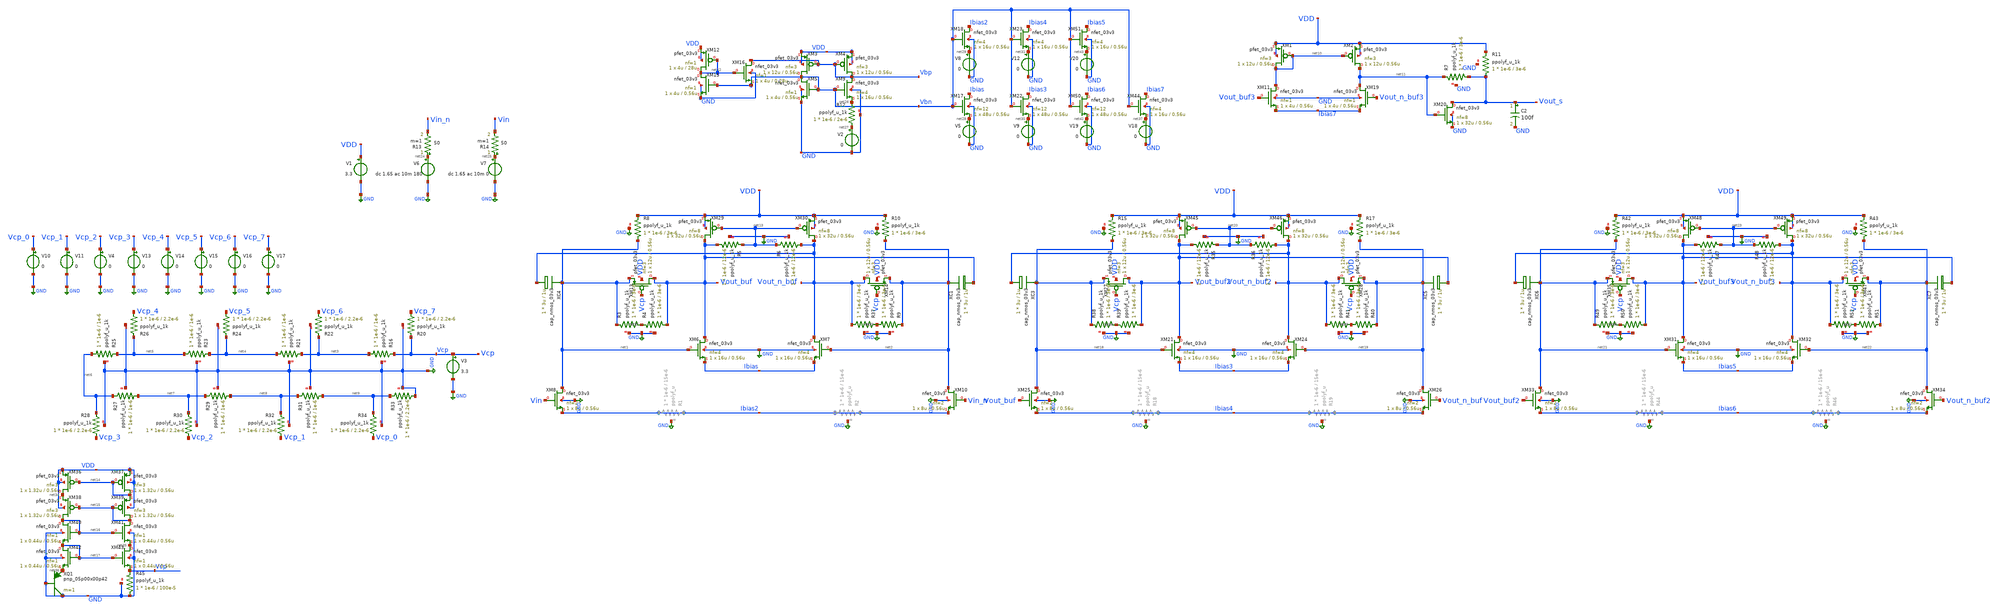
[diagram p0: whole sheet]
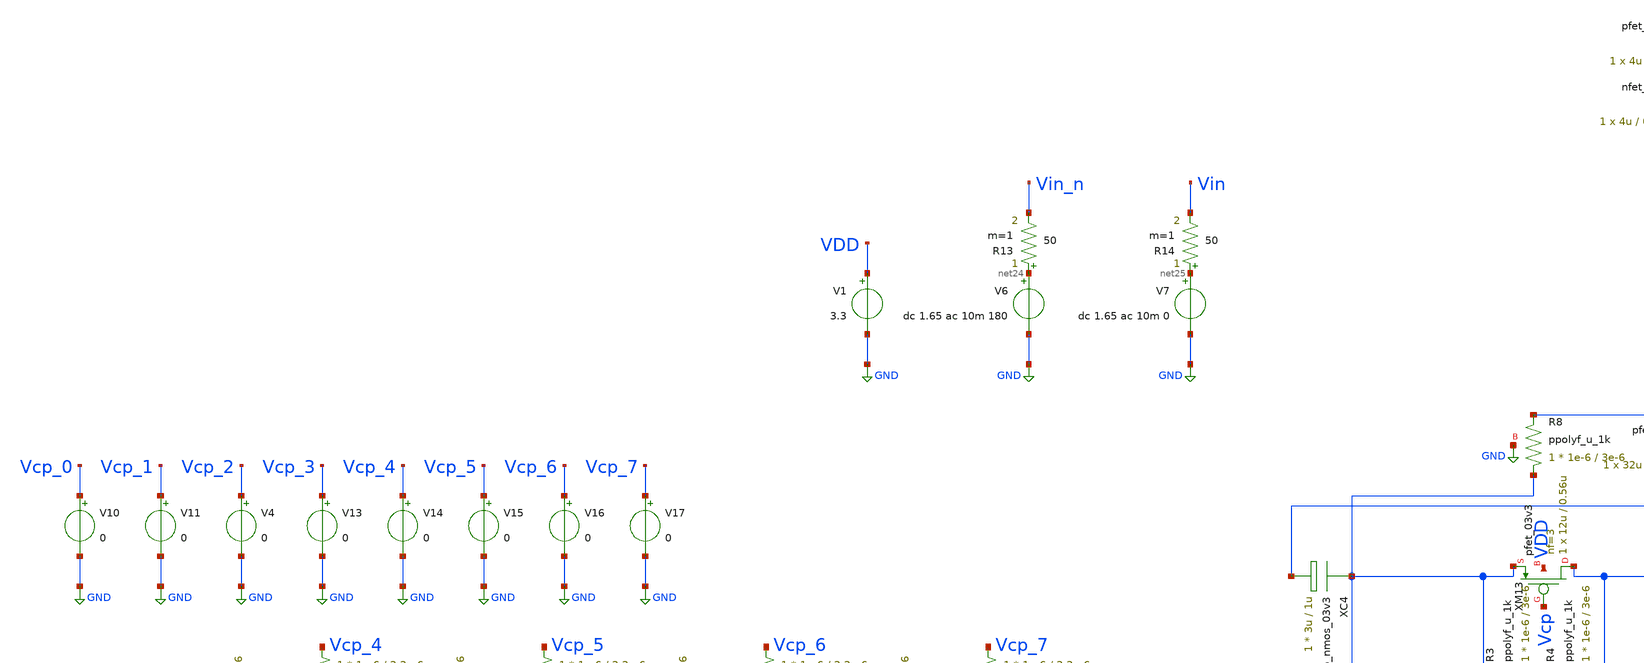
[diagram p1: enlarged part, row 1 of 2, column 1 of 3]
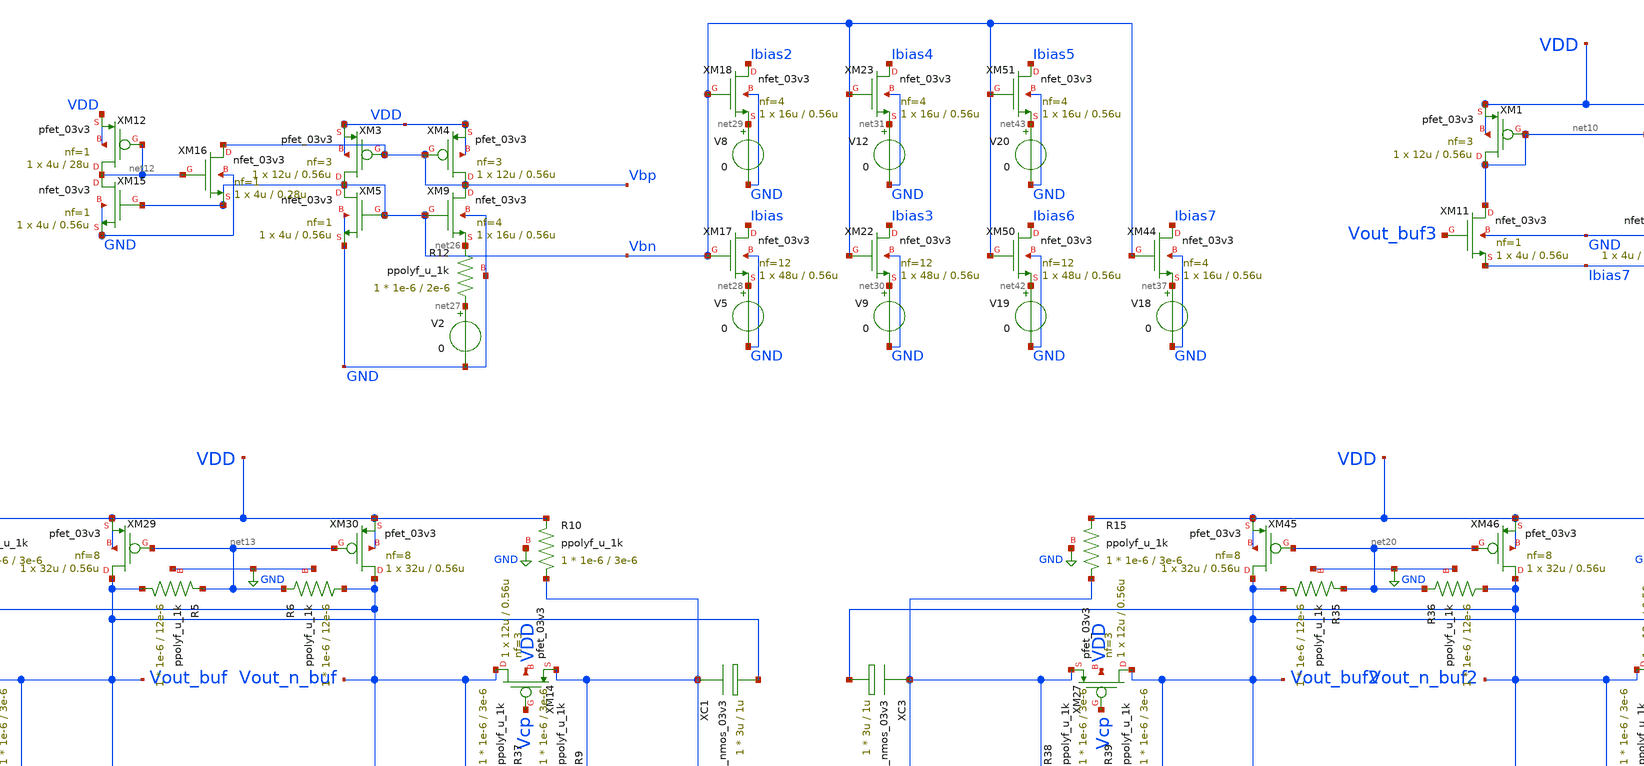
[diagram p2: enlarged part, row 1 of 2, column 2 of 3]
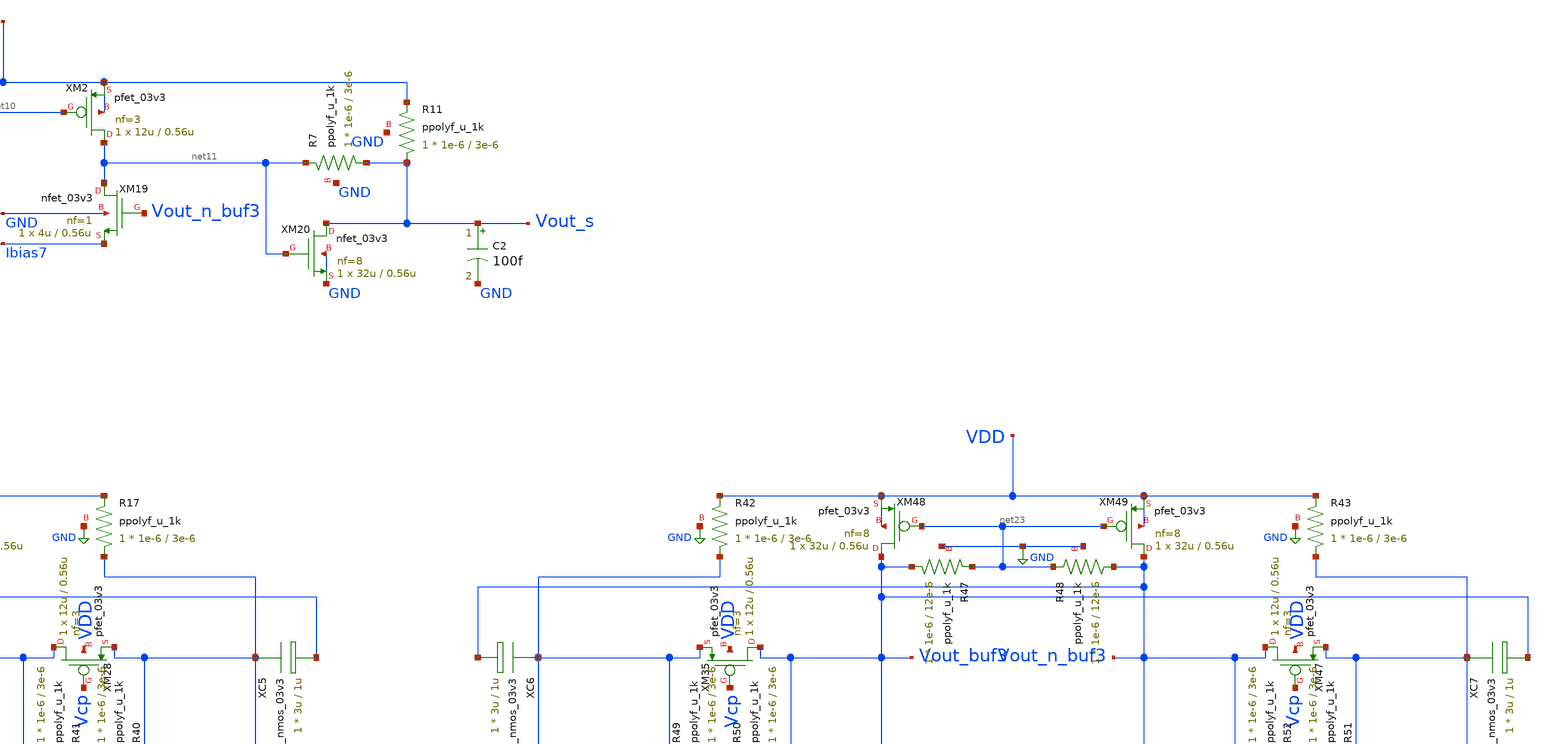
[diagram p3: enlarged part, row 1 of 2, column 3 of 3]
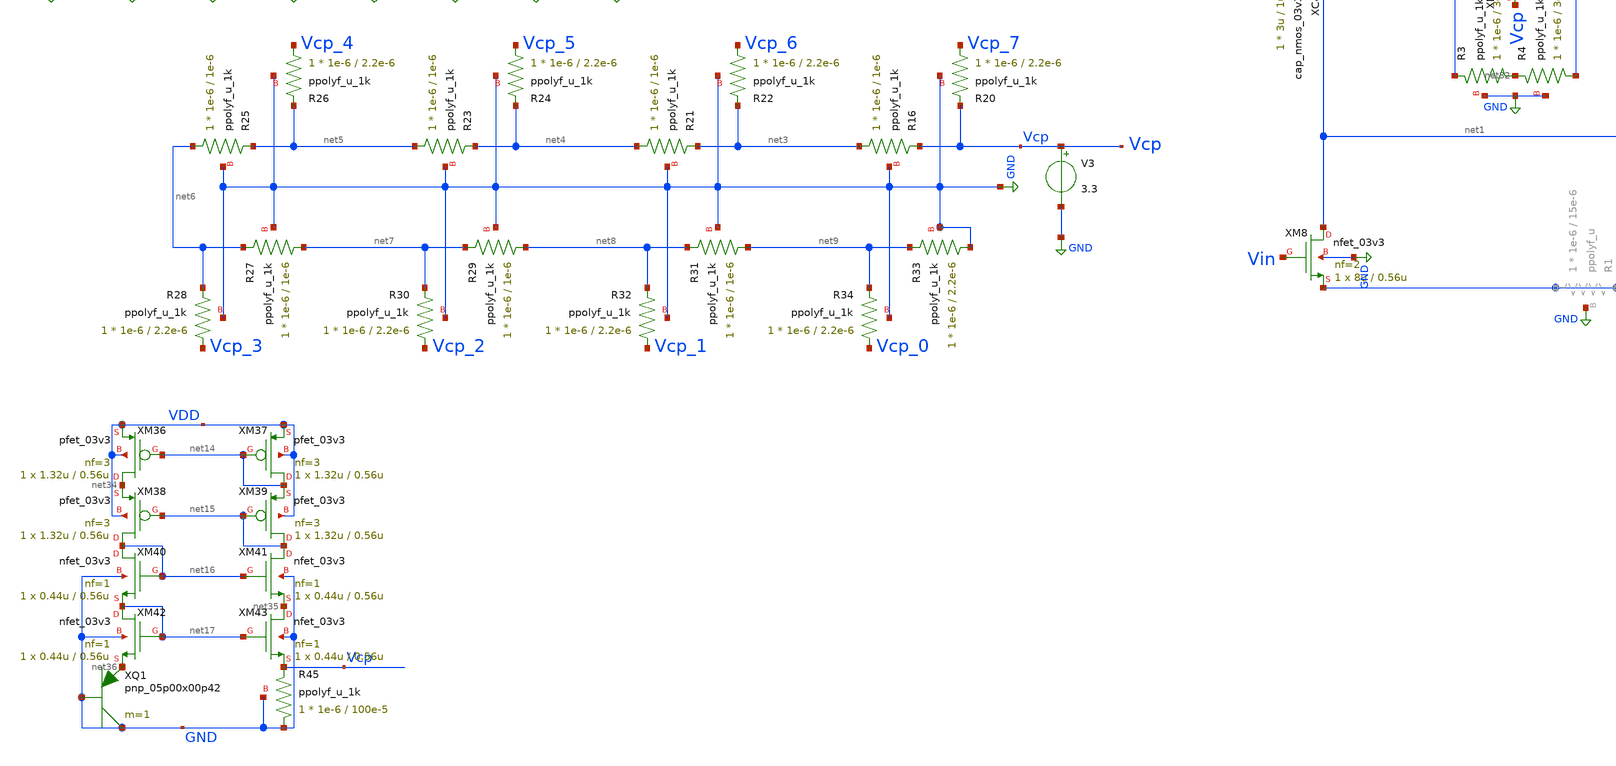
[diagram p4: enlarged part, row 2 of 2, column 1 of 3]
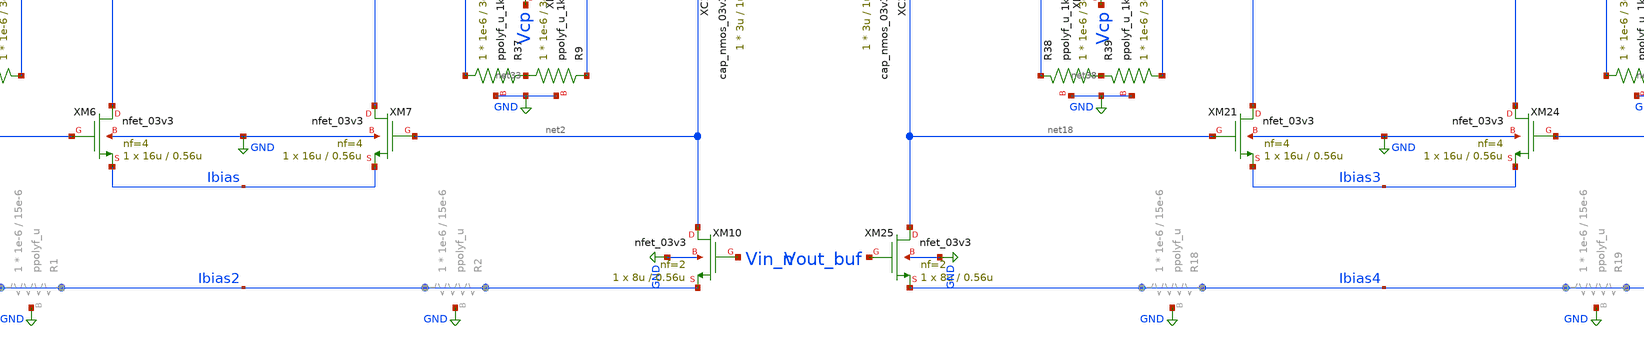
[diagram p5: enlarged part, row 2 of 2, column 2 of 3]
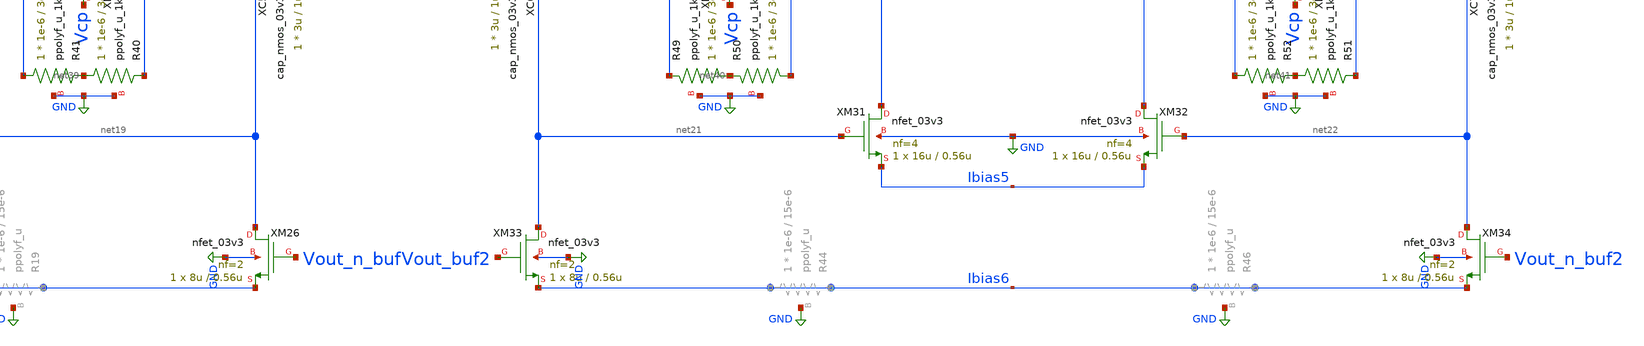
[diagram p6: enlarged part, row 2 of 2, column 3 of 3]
** sch_path: blocks/vga/vga.sch
**.subckt vga
V1 VDD GND 3.3
V6 net24 GND dc 1.65 ac 10m 180
XM6 Vout_buf net1 Ibias GND nfet_03v3 L=0.56u W=16u nf=4 ad='int((nf+1)/2) * W/nf * 0.18u' as='int((nf+2)/2) * W/nf * 0.18u'
+ pd='2*int((nf+1)/2) * (W/nf + 0.18u)' ps='2*int((nf+2)/2) * (W/nf + 0.18u)' nrd='0.18u / W' nrs='0.18u / W'
+ sa=0 sb=0 sd=0 m=1
XM7 Vout_n_buf net2 Ibias GND nfet_03v3 L=0.56u W=16u nf=4 ad='int((nf+1)/2) * W/nf * 0.18u' as='int((nf+2)/2) * W/nf * 0.18u'
+ pd='2*int((nf+1)/2) * (W/nf + 0.18u)' ps='2*int((nf+2)/2) * (W/nf + 0.18u)' nrd='0.18u / W' nrs='0.18u / W'
+ sa=0 sb=0 sd=0 m=1
XM8 net1 Vin Ibias2 GND nfet_03v3 L=0.56u W=8u nf=2 ad='int((nf+1)/2) * W/nf * 0.18u' as='int((nf+2)/2) * W/nf * 0.18u'
+ pd='2*int((nf+1)/2) * (W/nf + 0.18u)' ps='2*int((nf+2)/2) * (W/nf + 0.18u)' nrd='0.18u / W' nrs='0.18u / W'
+ sa=0 sb=0 sd=0 m=1
XM10 net2 Vin_n Ibias2 GND nfet_03v3 L=0.56u W=8u nf=2 ad='int((nf+1)/2) * W/nf * 0.18u' as='int((nf+2)/2) * W/nf * 0.18u'
+ pd='2*int((nf+1)/2) * (W/nf + 0.18u)' ps='2*int((nf+2)/2) * (W/nf + 0.18u)' nrd='0.18u / W' nrs='0.18u / W'
+ sa=0 sb=0 sd=0 m=1
V7 net25 GND dc 1.65 ac 10m 0
R14 net25 Vin 50 m=1
R13 net24 Vin_n 50 m=1
XR16 net3 Vcp GND ppolyf_u_1k r_width=1e-6 r_length=1e-6 m=1
XR20 Vcp_7 Vcp GND ppolyf_u_1k r_width=1e-6 r_length=2.2e-6 m=1
XR21 net4 net3 GND ppolyf_u_1k r_width=1e-6 r_length=1e-6 m=1
XR22 Vcp_6 net3 GND ppolyf_u_1k r_width=1e-6 r_length=2.2e-6 m=1
XR23 net5 net4 GND ppolyf_u_1k r_width=1e-6 r_length=1e-6 m=1
XR24 Vcp_5 net4 GND ppolyf_u_1k r_width=1e-6 r_length=2.2e-6 m=1
XR25 net6 net5 GND ppolyf_u_1k r_width=1e-6 r_length=1e-6 m=1
XR26 Vcp_4 net5 GND ppolyf_u_1k r_width=1e-6 r_length=2.2e-6 m=1
XR27 net7 net6 GND ppolyf_u_1k r_width=1e-6 r_length=1e-6 m=1
XR28 Vcp_3 net6 GND ppolyf_u_1k r_width=1e-6 r_length=2.2e-6 m=1
XR29 net8 net7 GND ppolyf_u_1k r_width=1e-6 r_length=1e-6 m=1
XR30 Vcp_2 net7 GND ppolyf_u_1k r_width=1e-6 r_length=2.2e-6 m=1
XR31 net9 net8 GND ppolyf_u_1k r_width=1e-6 r_length=1e-6 m=1
XR32 Vcp_1 net8 GND ppolyf_u_1k r_width=1e-6 r_length=2.2e-6 m=1
XR33 GND net9 GND ppolyf_u_1k r_width=1e-6 r_length=2.2e-6 m=1
XR34 Vcp_0 net9 GND ppolyf_u_1k r_width=1e-6 r_length=2.2e-6 m=1
V10 Vcp_0 GND 0
V11 Vcp_1 GND 0
V4 Vcp_2 GND 0
V13 Vcp_3 GND 0
V14 Vcp_4 GND 0
V15 Vcp_5 GND 0
V16 Vcp_6 GND 0
V17 Vcp_7 GND 0
V3 Vcp GND 3.3
XM13 Vout_buf Vcp net1 VDD pfet_03v3 L=0.56u W=12u nf=3 ad='int((nf+1)/2) * W/nf * 0.18u' as='int((nf+2)/2) * W/nf * 0.18u'
+ pd='2*int((nf+1)/2) * (W/nf + 0.18u)' ps='2*int((nf+2)/2) * (W/nf + 0.18u)' nrd='0.18u / W' nrs='0.18u / W'
+ sa=0 sb=0 sd=0 m=1
XM14 Vout_n_buf Vcp net2 VDD pfet_03v3 L=0.56u W=12u nf=3 ad='int((nf+1)/2) * W/nf * 0.18u' as='int((nf+2)/2) * W/nf * 0.18u'
+ pd='2*int((nf+1)/2) * (W/nf + 0.18u)' ps='2*int((nf+2)/2) * (W/nf + 0.18u)' nrd='0.18u / W' nrs='0.18u / W'
+ sa=0 sb=0 sd=0 m=1
XR8 net1 VDD GND ppolyf_u_1k r_width=1e-6 r_length=3e-6 m=1
XR10 net2 VDD GND ppolyf_u_1k r_width=1e-6 r_length=3e-6 m=1
XC4 net1 Vout_n_buf cap_nmos_03v3 c_width=3u c_length=1u m=1
XC1 net2 Vout_buf cap_nmos_03v3 c_width=3u c_length=1u m=1
XM11 net10 Vout_buf3 Ibias7 GND nfet_03v3 L=0.56u W=4u nf=1 ad='int((nf+1)/2) * W/nf * 0.18u' as='int((nf+2)/2) * W/nf * 0.18u'
+ pd='2*int((nf+1)/2) * (W/nf + 0.18u)' ps='2*int((nf+2)/2) * (W/nf + 0.18u)' nrd='0.18u / W' nrs='0.18u / W'
+ sa=0 sb=0 sd=0 m=1
XM19 net11 Vout_n_buf3 Ibias7 GND nfet_03v3 L=0.56u W=4u nf=1 ad='int((nf+1)/2) * W/nf * 0.18u' as='int((nf+2)/2) * W/nf * 0.18u'
+ pd='2*int((nf+1)/2) * (W/nf + 0.18u)' ps='2*int((nf+2)/2) * (W/nf + 0.18u)' nrd='0.18u / W' nrs='0.18u / W'
+ sa=0 sb=0 sd=0 m=1
XR7 Vout_s net11 GND ppolyf_u_1k r_width=1e-6 r_length=3e-6 m=1
XM20 Vout_s net11 GND GND nfet_03v3 L=0.56u W=32u nf=8 ad='int((nf+1)/2) * W/nf * 0.18u' as='int((nf+2)/2) * W/nf * 0.18u'
+ pd='2*int((nf+1)/2) * (W/nf + 0.18u)' ps='2*int((nf+2)/2) * (W/nf + 0.18u)' nrd='0.18u / W' nrs='0.18u / W'
+ sa=0 sb=0 sd=0 m=1
C2 Vout_s GND 100f m=1
XR11 Vout_s VDD GND ppolyf_u_1k r_width=1e-6 r_length=3e-6 m=1
XM1 net10 net10 VDD VDD pfet_03v3 L=0.56u W=12u nf=3 ad='int((nf+1)/2) * W/nf * 0.18u' as='int((nf+2)/2) * W/nf * 0.18u'
+ pd='2*int((nf+1)/2) * (W/nf + 0.18u)' ps='2*int((nf+2)/2) * (W/nf + 0.18u)' nrd='0.18u / W' nrs='0.18u / W'
+ sa=0 sb=0 sd=0 m=1
XM2 net11 net10 VDD VDD pfet_03v3 L=0.56u W=12u nf=3 ad='int((nf+1)/2) * W/nf * 0.18u' as='int((nf+2)/2) * W/nf * 0.18u'
+ pd='2*int((nf+1)/2) * (W/nf + 0.18u)' ps='2*int((nf+2)/2) * (W/nf + 0.18u)' nrd='0.18u / W' nrs='0.18u / W'
+ sa=0 sb=0 sd=0 m=1
XM3 Vbn Vbp VDD VDD pfet_03v3 L=0.56u W=12u nf=3 ad='int((nf+1)/2) * W/nf * 0.18u' as='int((nf+2)/2) * W/nf * 0.18u'
+ pd='2*int((nf+1)/2) * (W/nf + 0.18u)' ps='2*int((nf+2)/2) * (W/nf + 0.18u)' nrd='0.18u / W' nrs='0.18u / W'
+ sa=0 sb=0 sd=0 m=1
XM4 Vbp Vbp VDD VDD pfet_03v3 L=0.56u W=12u nf=3 ad='int((nf+1)/2) * W/nf * 0.18u' as='int((nf+2)/2) * W/nf * 0.18u'
+ pd='2*int((nf+1)/2) * (W/nf + 0.18u)' ps='2*int((nf+2)/2) * (W/nf + 0.18u)' nrd='0.18u / W' nrs='0.18u / W'
+ sa=0 sb=0 sd=0 m=1
XM5 Vbn Vbn GND GND nfet_03v3 L=0.56u W=4u nf=1 ad='int((nf+1)/2) * W/nf * 0.18u' as='int((nf+2)/2) * W/nf * 0.18u'
+ pd='2*int((nf+1)/2) * (W/nf + 0.18u)' ps='2*int((nf+2)/2) * (W/nf + 0.18u)' nrd='0.18u / W' nrs='0.18u / W'
+ sa=0 sb=0 sd=0 m=1
XM9 Vbp Vbn net26 GND nfet_03v3 L=0.56u W=16u nf=4 ad='int((nf+1)/2) * W/nf * 0.18u' as='int((nf+2)/2) * W/nf * 0.18u'
+ pd='2*int((nf+1)/2) * (W/nf + 0.18u)' ps='2*int((nf+2)/2) * (W/nf + 0.18u)' nrd='0.18u / W' nrs='0.18u / W'
+ sa=0 sb=0 sd=0 m=1
XM12 net12 net12 VDD VDD pfet_03v3 L=28u W=4u nf=1 ad='int((nf+1)/2) * W/nf * 0.18u' as='int((nf+2)/2) * W/nf * 0.18u'
+ pd='2*int((nf+1)/2) * (W/nf + 0.18u)' ps='2*int((nf+2)/2) * (W/nf + 0.18u)' nrd='0.18u / W' nrs='0.18u / W'
+ sa=0 sb=0 sd=0 m=1
XM15 net12 Vbn GND GND nfet_03v3 L=0.56u W=4u nf=1 ad='int((nf+1)/2) * W/nf * 0.18u' as='int((nf+2)/2) * W/nf * 0.18u'
+ pd='2*int((nf+1)/2) * (W/nf + 0.18u)' ps='2*int((nf+2)/2) * (W/nf + 0.18u)' nrd='0.18u / W' nrs='0.18u / W'
+ sa=0 sb=0 sd=0 m=1
XM16 Vbp net12 Vbn GND nfet_03v3 L=0.28u W=4u nf=1 ad='int((nf+1)/2) * W/nf * 0.18u' as='int((nf+2)/2) * W/nf * 0.18u'
+ pd='2*int((nf+1)/2) * (W/nf + 0.18u)' ps='2*int((nf+2)/2) * (W/nf + 0.18u)' nrd='0.18u / W' nrs='0.18u / W'
+ sa=0 sb=0 sd=0 m=1
XR12 net27 net26 GND ppolyf_u_1k r_width=1e-6 r_length=2e-6 m=1
V2 net27 GND 0
XM17 Ibias Vbn net28 GND nfet_03v3 L=0.56u W=48u nf=12 ad='int((nf+1)/2) * W/nf * 0.18u' as='int((nf+2)/2) * W/nf * 0.18u'
+ pd='2*int((nf+1)/2) * (W/nf + 0.18u)' ps='2*int((nf+2)/2) * (W/nf + 0.18u)' nrd='0.18u / W' nrs='0.18u / W'
+ sa=0 sb=0 sd=0 m=1
V5 net28 GND 0
XM18 Ibias2 Vbn net29 GND nfet_03v3 L=0.56u W=16u nf=4 ad='int((nf+1)/2) * W/nf * 0.18u' as='int((nf+2)/2) * W/nf * 0.18u'
+ pd='2*int((nf+1)/2) * (W/nf + 0.18u)' ps='2*int((nf+2)/2) * (W/nf + 0.18u)' nrd='0.18u / W' nrs='0.18u / W'
+ sa=0 sb=0 sd=0 m=1
V8 net29 GND 0
XM22 Ibias3 Vbn net30 GND nfet_03v3 L=0.56u W=48u nf=12 ad='int((nf+1)/2) * W/nf * 0.18u' as='int((nf+2)/2) * W/nf * 0.18u'
+ pd='2*int((nf+1)/2) * (W/nf + 0.18u)' ps='2*int((nf+2)/2) * (W/nf + 0.18u)' nrd='0.18u / W' nrs='0.18u / W'
+ sa=0 sb=0 sd=0 m=1
V9 net30 GND 0
XM23 Ibias4 Vbn net31 GND nfet_03v3 L=0.56u W=16u nf=4 ad='int((nf+1)/2) * W/nf * 0.18u' as='int((nf+2)/2) * W/nf * 0.18u'
+ pd='2*int((nf+1)/2) * (W/nf + 0.18u)' ps='2*int((nf+2)/2) * (W/nf + 0.18u)' nrd='0.18u / W' nrs='0.18u / W'
+ sa=0 sb=0 sd=0 m=1
V12 net31 GND 0
XM29 Vout_buf net13 VDD VDD pfet_03v3 L=0.56u W=32u nf=8 ad='int((nf+1)/2) * W/nf * 0.18u' as='int((nf+2)/2) * W/nf * 0.18u'
+ pd='2*int((nf+1)/2) * (W/nf + 0.18u)' ps='2*int((nf+2)/2) * (W/nf + 0.18u)' nrd='0.18u / W' nrs='0.18u / W'
+ sa=0 sb=0 sd=0 m=1
XM30 Vout_n_buf net13 VDD VDD pfet_03v3 L=0.56u W=32u nf=8 ad='int((nf+1)/2) * W/nf * 0.18u' as='int((nf+2)/2) * W/nf * 0.18u'
+ pd='2*int((nf+1)/2) * (W/nf + 0.18u)' ps='2*int((nf+2)/2) * (W/nf + 0.18u)' nrd='0.18u / W' nrs='0.18u / W'
+ sa=0 sb=0 sd=0 m=1
XR5 Vout_buf net13 GND ppolyf_u_1k r_width=1e-6 r_length=12e-6 m=1
XR6 Vout_n_buf net13 GND ppolyf_u_1k r_width=1e-6 r_length=12e-6 m=1
XR3 net32 net1 GND ppolyf_u_1k r_width=1e-6 r_length=3e-6 m=1
XR4 Vout_buf net32 GND ppolyf_u_1k r_width=1e-6 r_length=3e-6 m=1
XR9 net33 net2 GND ppolyf_u_1k r_width=1e-6 r_length=3e-6 m=1
XR37 Vout_n_buf net33 GND ppolyf_u_1k r_width=1e-6 r_length=3e-6 m=1
XM36 net34 net14 VDD VDD pfet_03v3 L=0.56u W=1.32u nf=3 ad='int((nf+1)/2) * W/nf * 0.18u' as='int((nf+2)/2) * W/nf * 0.18u'
+ pd='2*int((nf+1)/2) * (W/nf + 0.18u)' ps='2*int((nf+2)/2) * (W/nf + 0.18u)' nrd='0.18u / W' nrs='0.18u / W'
+ sa=0 sb=0 sd=0 m=1
XM37 net14 net14 VDD VDD pfet_03v3 L=0.56u W=1.32u nf=3 ad='int((nf+1)/2) * W/nf * 0.18u' as='int((nf+2)/2) * W/nf * 0.18u'
+ pd='2*int((nf+1)/2) * (W/nf + 0.18u)' ps='2*int((nf+2)/2) * (W/nf + 0.18u)' nrd='0.18u / W' nrs='0.18u / W'
+ sa=0 sb=0 sd=0 m=1
XM38 net16 net15 net34 VDD pfet_03v3 L=0.56u W=1.32u nf=3 ad='int((nf+1)/2) * W/nf * 0.18u' as='int((nf+2)/2) * W/nf * 0.18u'
+ pd='2*int((nf+1)/2) * (W/nf + 0.18u)' ps='2*int((nf+2)/2) * (W/nf + 0.18u)' nrd='0.18u / W' nrs='0.18u / W'
+ sa=0 sb=0 sd=0 m=1
XM39 net15 net15 net14 VDD pfet_03v3 L=0.56u W=1.32u nf=3 ad='int((nf+1)/2) * W/nf * 0.18u' as='int((nf+2)/2) * W/nf * 0.18u'
+ pd='2*int((nf+1)/2) * (W/nf + 0.18u)' ps='2*int((nf+2)/2) * (W/nf + 0.18u)' nrd='0.18u / W' nrs='0.18u / W'
+ sa=0 sb=0 sd=0 m=1
XM40 net16 net16 net17 GND nfet_03v3 L=0.56u W=0.44u nf=1 ad='int((nf+1)/2) * W/nf * 0.18u' as='int((nf+2)/2) * W/nf * 0.18u'
+ pd='2*int((nf+1)/2) * (W/nf + 0.18u)' ps='2*int((nf+2)/2) * (W/nf + 0.18u)' nrd='0.18u / W' nrs='0.18u / W'
+ sa=0 sb=0 sd=0 m=1
XM41 net15 net16 net35 GND nfet_03v3 L=0.56u W=0.44u nf=1 ad='int((nf+1)/2) * W/nf * 0.18u' as='int((nf+2)/2) * W/nf * 0.18u'
+ pd='2*int((nf+1)/2) * (W/nf + 0.18u)' ps='2*int((nf+2)/2) * (W/nf + 0.18u)' nrd='0.18u / W' nrs='0.18u / W'
+ sa=0 sb=0 sd=0 m=1
XM42 net17 net17 net36 GND nfet_03v3 L=0.56u W=0.44u nf=1 ad='int((nf+1)/2) * W/nf * 0.18u' as='int((nf+2)/2) * W/nf * 0.18u'
+ pd='2*int((nf+1)/2) * (W/nf + 0.18u)' ps='2*int((nf+2)/2) * (W/nf + 0.18u)' nrd='0.18u / W' nrs='0.18u / W'
+ sa=0 sb=0 sd=0 m=1
XM43 net35 net17 Vcp GND nfet_03v3 L=0.56u W=0.44u nf=1 ad='int((nf+1)/2) * W/nf * 0.18u' as='int((nf+2)/2) * W/nf * 0.18u'
+ pd='2*int((nf+1)/2) * (W/nf + 0.18u)' ps='2*int((nf+2)/2) * (W/nf + 0.18u)' nrd='0.18u / W' nrs='0.18u / W'
+ sa=0 sb=0 sd=0 m=1
XQ1 GND GND net36 pnp_05p00x00p42 m=1 par=1
XR45 GND Vcp GND ppolyf_u_1k r_width=1e-6 r_length=100e-5 m=1
XM44 Ibias7 Vbn net37 GND nfet_03v3 L=0.56u W=16u nf=4 ad='int((nf+1)/2) * W/nf * 0.18u' as='int((nf+2)/2) * W/nf * 0.18u'
+ pd='2*int((nf+1)/2) * (W/nf + 0.18u)' ps='2*int((nf+2)/2) * (W/nf + 0.18u)' nrd='0.18u / W' nrs='0.18u / W'
+ sa=0 sb=0 sd=0 m=1
V18 net37 GND 0
XM21 Vout_buf2 net18 Ibias3 GND nfet_03v3 L=0.56u W=16u nf=4 ad='int((nf+1)/2) * W/nf * 0.18u' as='int((nf+2)/2) * W/nf * 0.18u'
+ pd='2*int((nf+1)/2) * (W/nf + 0.18u)' ps='2*int((nf+2)/2) * (W/nf + 0.18u)' nrd='0.18u / W' nrs='0.18u / W'
+ sa=0 sb=0 sd=0 m=1
XM24 Vout_n_buf2 net19 Ibias3 GND nfet_03v3 L=0.56u W=16u nf=4 ad='int((nf+1)/2) * W/nf * 0.18u' as='int((nf+2)/2) * W/nf * 0.18u'
+ pd='2*int((nf+1)/2) * (W/nf + 0.18u)' ps='2*int((nf+2)/2) * (W/nf + 0.18u)' nrd='0.18u / W' nrs='0.18u / W'
+ sa=0 sb=0 sd=0 m=1
XM25 net18 Vout_buf Ibias4 GND nfet_03v3 L=0.56u W=8u nf=2 ad='int((nf+1)/2) * W/nf * 0.18u' as='int((nf+2)/2) * W/nf * 0.18u'
+ pd='2*int((nf+1)/2) * (W/nf + 0.18u)' ps='2*int((nf+2)/2) * (W/nf + 0.18u)' nrd='0.18u / W' nrs='0.18u / W'
+ sa=0 sb=0 sd=0 m=1
XM26 net19 Vout_n_buf Ibias4 GND nfet_03v3 L=0.56u W=8u nf=2 ad='int((nf+1)/2) * W/nf * 0.18u' as='int((nf+2)/2) * W/nf * 0.18u'
+ pd='2*int((nf+1)/2) * (W/nf + 0.18u)' ps='2*int((nf+2)/2) * (W/nf + 0.18u)' nrd='0.18u / W' nrs='0.18u / W'
+ sa=0 sb=0 sd=0 m=1
XM27 Vout_buf2 Vcp net18 VDD pfet_03v3 L=0.56u W=12u nf=3 ad='int((nf+1)/2) * W/nf * 0.18u' as='int((nf+2)/2) * W/nf * 0.18u'
+ pd='2*int((nf+1)/2) * (W/nf + 0.18u)' ps='2*int((nf+2)/2) * (W/nf + 0.18u)' nrd='0.18u / W' nrs='0.18u / W'
+ sa=0 sb=0 sd=0 m=1
XM28 Vout_n_buf2 Vcp net19 VDD pfet_03v3 L=0.56u W=12u nf=3 ad='int((nf+1)/2) * W/nf * 0.18u' as='int((nf+2)/2) * W/nf * 0.18u'
+ pd='2*int((nf+1)/2) * (W/nf + 0.18u)' ps='2*int((nf+2)/2) * (W/nf + 0.18u)' nrd='0.18u / W' nrs='0.18u / W'
+ sa=0 sb=0 sd=0 m=1
XR15 net18 VDD GND ppolyf_u_1k r_width=1e-6 r_length=3e-6 m=1
XR17 net19 VDD GND ppolyf_u_1k r_width=1e-6 r_length=3e-6 m=1
XC3 net18 Vout_n_buf2 cap_nmos_03v3 c_width=3u c_length=1u m=1
XC5 net19 Vout_buf2 cap_nmos_03v3 c_width=3u c_length=1u m=1
XM45 Vout_buf2 net20 VDD VDD pfet_03v3 L=0.56u W=32u nf=8 ad='int((nf+1)/2) * W/nf * 0.18u' as='int((nf+2)/2) * W/nf * 0.18u'
+ pd='2*int((nf+1)/2) * (W/nf + 0.18u)' ps='2*int((nf+2)/2) * (W/nf + 0.18u)' nrd='0.18u / W' nrs='0.18u / W'
+ sa=0 sb=0 sd=0 m=1
XM46 Vout_n_buf2 net20 VDD VDD pfet_03v3 L=0.56u W=32u nf=8 ad='int((nf+1)/2) * W/nf * 0.18u' as='int((nf+2)/2) * W/nf * 0.18u'
+ pd='2*int((nf+1)/2) * (W/nf + 0.18u)' ps='2*int((nf+2)/2) * (W/nf + 0.18u)' nrd='0.18u / W' nrs='0.18u / W'
+ sa=0 sb=0 sd=0 m=1
XR35 Vout_buf2 net20 GND ppolyf_u_1k r_width=1e-6 r_length=12e-6 m=1
XR36 Vout_n_buf2 net20 GND ppolyf_u_1k r_width=1e-6 r_length=12e-6 m=1
XR38 net38 net18 GND ppolyf_u_1k r_width=1e-6 r_length=3e-6 m=1
XR39 Vout_buf2 net38 GND ppolyf_u_1k r_width=1e-6 r_length=3e-6 m=1
XR40 net39 net19 GND ppolyf_u_1k r_width=1e-6 r_length=3e-6 m=1
XR41 Vout_n_buf2 net39 GND ppolyf_u_1k r_width=1e-6 r_length=3e-6 m=1
XM31 Vout_buf3 net21 Ibias5 GND nfet_03v3 L=0.56u W=16u nf=4 ad='int((nf+1)/2) * W/nf * 0.18u' as='int((nf+2)/2) * W/nf * 0.18u'
+ pd='2*int((nf+1)/2) * (W/nf + 0.18u)' ps='2*int((nf+2)/2) * (W/nf + 0.18u)' nrd='0.18u / W' nrs='0.18u / W'
+ sa=0 sb=0 sd=0 m=1
XM32 Vout_n_buf3 net22 Ibias5 GND nfet_03v3 L=0.56u W=16u nf=4 ad='int((nf+1)/2) * W/nf * 0.18u' as='int((nf+2)/2) * W/nf * 0.18u'
+ pd='2*int((nf+1)/2) * (W/nf + 0.18u)' ps='2*int((nf+2)/2) * (W/nf + 0.18u)' nrd='0.18u / W' nrs='0.18u / W'
+ sa=0 sb=0 sd=0 m=1
XM33 net21 Vout_buf2 Ibias6 GND nfet_03v3 L=0.56u W=8u nf=2 ad='int((nf+1)/2) * W/nf * 0.18u' as='int((nf+2)/2) * W/nf * 0.18u'
+ pd='2*int((nf+1)/2) * (W/nf + 0.18u)' ps='2*int((nf+2)/2) * (W/nf + 0.18u)' nrd='0.18u / W' nrs='0.18u / W'
+ sa=0 sb=0 sd=0 m=1
XM34 net22 Vout_n_buf2 Ibias6 GND nfet_03v3 L=0.56u W=8u nf=2 ad='int((nf+1)/2) * W/nf * 0.18u' as='int((nf+2)/2) * W/nf * 0.18u'
+ pd='2*int((nf+1)/2) * (W/nf + 0.18u)' ps='2*int((nf+2)/2) * (W/nf + 0.18u)' nrd='0.18u / W' nrs='0.18u / W'
+ sa=0 sb=0 sd=0 m=1
XM35 Vout_buf3 Vcp net21 VDD pfet_03v3 L=0.56u W=12u nf=3 ad='int((nf+1)/2) * W/nf * 0.18u' as='int((nf+2)/2) * W/nf * 0.18u'
+ pd='2*int((nf+1)/2) * (W/nf + 0.18u)' ps='2*int((nf+2)/2) * (W/nf + 0.18u)' nrd='0.18u / W' nrs='0.18u / W'
+ sa=0 sb=0 sd=0 m=1
XM47 Vout_n_buf3 Vcp net22 VDD pfet_03v3 L=0.56u W=12u nf=3 ad='int((nf+1)/2) * W/nf * 0.18u' as='int((nf+2)/2) * W/nf * 0.18u'
+ pd='2*int((nf+1)/2) * (W/nf + 0.18u)' ps='2*int((nf+2)/2) * (W/nf + 0.18u)' nrd='0.18u / W' nrs='0.18u / W'
+ sa=0 sb=0 sd=0 m=1
XR42 net21 VDD GND ppolyf_u_1k r_width=1e-6 r_length=3e-6 m=1
XR43 net22 VDD GND ppolyf_u_1k r_width=1e-6 r_length=3e-6 m=1
XC6 net21 Vout_n_buf3 cap_nmos_03v3 c_width=3u c_length=1u m=1
XC7 net22 Vout_buf3 cap_nmos_03v3 c_width=3u c_length=1u m=1
XM48 Vout_buf3 net23 VDD VDD pfet_03v3 L=0.56u W=32u nf=8 ad='int((nf+1)/2) * W/nf * 0.18u' as='int((nf+2)/2) * W/nf * 0.18u'
+ pd='2*int((nf+1)/2) * (W/nf + 0.18u)' ps='2*int((nf+2)/2) * (W/nf + 0.18u)' nrd='0.18u / W' nrs='0.18u / W'
+ sa=0 sb=0 sd=0 m=1
XM49 Vout_n_buf3 net23 VDD VDD pfet_03v3 L=0.56u W=32u nf=8 ad='int((nf+1)/2) * W/nf * 0.18u' as='int((nf+2)/2) * W/nf * 0.18u'
+ pd='2*int((nf+1)/2) * (W/nf + 0.18u)' ps='2*int((nf+2)/2) * (W/nf + 0.18u)' nrd='0.18u / W' nrs='0.18u / W'
+ sa=0 sb=0 sd=0 m=1
XR47 Vout_buf3 net23 GND ppolyf_u_1k r_width=1e-6 r_length=12e-6 m=1
XR48 Vout_n_buf3 net23 GND ppolyf_u_1k r_width=1e-6 r_length=12e-6 m=1
XR49 net40 net21 GND ppolyf_u_1k r_width=1e-6 r_length=3e-6 m=1
XR50 Vout_buf3 net40 GND ppolyf_u_1k r_width=1e-6 r_length=3e-6 m=1
XR51 net41 net22 GND ppolyf_u_1k r_width=1e-6 r_length=3e-6 m=1
XR52 Vout_n_buf3 net41 GND ppolyf_u_1k r_width=1e-6 r_length=3e-6 m=1
XM50 Ibias6 Vbn net42 GND nfet_03v3 L=0.56u W=48u nf=12 ad='int((nf+1)/2) * W/nf * 0.18u' as='int((nf+2)/2) * W/nf * 0.18u'
+ pd='2*int((nf+1)/2) * (W/nf + 0.18u)' ps='2*int((nf+2)/2) * (W/nf + 0.18u)' nrd='0.18u / W' nrs='0.18u / W'
+ sa=0 sb=0 sd=0 m=1
V19 net42 GND 0
XM51 Ibias5 Vbn net43 GND nfet_03v3 L=0.56u W=16u nf=4 ad='int((nf+1)/2) * W/nf * 0.18u' as='int((nf+2)/2) * W/nf * 0.18u'
+ pd='2*int((nf+1)/2) * (W/nf + 0.18u)' ps='2*int((nf+2)/2) * (W/nf + 0.18u)' nrd='0.18u / W' nrs='0.18u / W'
+ sa=0 sb=0 sd=0 m=1
V20 net43 GND 0
**** begin user architecture code


.include /foss/pdks/gf180mcuD/libs.tech/ngspice/design.ngspice
.lib /foss/pdks/gf180mcuD/libs.tech/ngspice/sm141064.ngspice ff
.lib /foss/pdks/gf180mcuD/libs.tech/ngspice/sm141064.ngspice bjt_ff
.lib /foss/pdks/gf180mcuD/libs.tech/ngspice/sm141064.ngspice diode_ff
.lib /foss/pdks/gf180mcuD/libs.tech/ngspice/sm141064.ngspice res_ff
.lib /foss/pdks/gf180mcuD/libs.tech/ngspice/sm141064.ngspice mimcap_ff
.lib /foss/pdks/gf180mcuD/libs.tech/ngspice/sm141064.ngspice moscap_ff
.option method=gear

.control
set temp = 85
  * 1. Setup the sweep parameters
  let v_ctrl = 3.3

  let f_start = 1
  let f_stop = 3.2G
  let f_points = 120

  * 2. Initialize vectors to store results
  let gain_db = unitvec(f_points)

  alter v3 = v_ctrl
  ac dec $&f_points $&f_start $&f_stop

  * 4. Calculate Differential Gain in dB
  * Formula: 20 * log10(|Vout_diff| / |Vin_diff|)
  let vin_mag = mag(v(vin) - v(vin_n))
  let vout_s_mag = mag(v(vout_s))
  let vout_buf_mag = mag(v(vout_buf2) - v(vout_n_buf2))
  let vout_s_gain = 20 * log10(vout_s_mag / vin_mag)
  let vout_buf_gain = 20 * log10(vout_buf_mag / vin_mag)

  * Credit to marcel hendrix
  * https://sourceforge.net/p/ngspice/discussion/133842/thread/2031ad61/
  meas ac peak  MAX  vmag(vout_s) FROM=$&f_start TO=$&f_stop
  let f3db = peak/sqrt(2)
  meas ac lo_3db WHEN vmag(vout_s)=f3db RISE=1
  meas ac hi_3db WHEN vmag(vout_s)=f3db FALL=1

  meas ac peak  MAX  vout_buf_mag FROM=$&f_start TO=$&f_stop
  let f3db = peak/sqrt(2)
  meas ac lo_3db WHEN vout_buf_mag=f3db RISE=1
  meas ac hi_3db WHEN vout_buf_mag=f3db FALL=1

  * 5. Save results to vectors
  plot vout_s_gain vout_buf_gain title 'Gain (dB) vs. Frequency from 1MHz to 3.2GHz, 0.6 vctrl' ylimit
+ -20 60
.endc


**** end user architecture code
**.ends
.GLOBAL GND
.end
